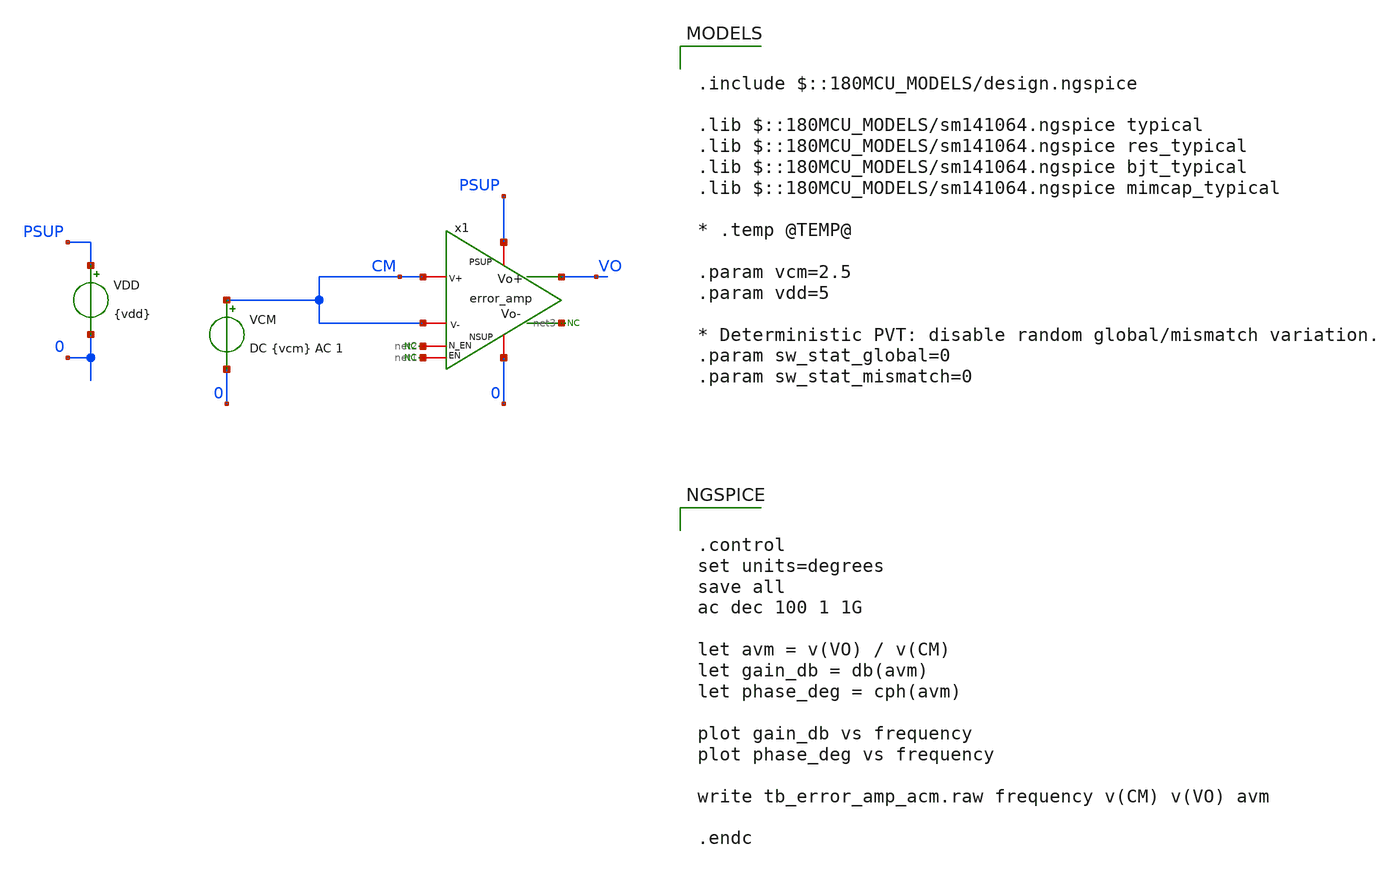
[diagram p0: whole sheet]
** sch_path: xschem/blocks/error_amp/tb_error_amp_acm.sch
**.subckt tb_error_amp_acm
VDD PSUP 0 {vdd}
VCM CM 0 DC {vcm} AC 1
* noconn #net1
* noconn #net2
x1 PSUP CM CM net2 0 net1 net3 VO error_amp
* noconn #net3
**** begin user architecture code

.include $::180MCU_MODELS/design.ngspice

.lib $::180MCU_MODELS/sm141064.ngspice typical
.lib $::180MCU_MODELS/sm141064.ngspice res_typical
.lib $::180MCU_MODELS/sm141064.ngspice bjt_typical
.lib $::180MCU_MODELS/sm141064.ngspice mimcap_typical

* .temp @TEMP@

.param vcm=2.5
.param vdd=5

* Deterministic PVT: disable random global/mismatch variation.
.param sw_stat_global=0
.param sw_stat_mismatch=0



.control
set units=degrees
save all
ac dec 100 1 1G

let avm = v(VO) / v(CM)
let gain_db = db(avm)
let phase_deg = cph(avm)

plot gain_db vs frequency
plot phase_deg vs frequency

write tb_error_amp_acm.raw frequency v(CM) v(VO) avm

.endc


**** end user architecture code
**.ends

* expanding   symbol:  blocks/error_amp/error_amp.sym # of pins=8
** sym_path: xschem/blocks/error_amp/error_amp.sym
** sch_path: xschem/blocks/error_amp/error_amp.sch
.subckt error_amp PSUP V+ V- N_EN NSUP EN Vo- Vo+
*.ipin PSUP
*.ipin NSUP
*.ipin N_EN
*.ipin EN
*.ipin V+
*.ipin V-
*.opin Vo-
*.opin Vo+
XM5 AA1 vb1 PSUP PSUP pfet_06v0 L=4u W=2u nf=4 ad='int((nf+1)/2) * W/nf * 0.18u' as='int((nf+2)/2) * W/nf * 0.18u'
+ pd='2*int((nf+1)/2) * (W/nf + 0.18u)' ps='2*int((nf+2)/2) * (W/nf + 0.18u)' nrd='0.18u / W' nrs='0.18u / W'
+ sa=0 sb=0 sd=0 m=2
XM6 AA2 vb1 PSUP PSUP pfet_06v0 L=4u W=2u nf=4 ad='int((nf+1)/2) * W/nf * 0.18u' as='int((nf+2)/2) * W/nf * 0.18u'
+ pd='2*int((nf+1)/2) * (W/nf + 0.18u)' ps='2*int((nf+2)/2) * (W/nf + 0.18u)' nrd='0.18u / W' nrs='0.18u / W'
+ sa=0 sb=0 sd=0 m=2
* noconn N_EN
* noconn EN
XM1 AA4 V- AA5 NSUP nfet_06v0 L=2u W=4u nf=5 ad='int((nf+1)/2) * W/nf * 0.18u' as='int((nf+2)/2) * W/nf * 0.18u'
+ pd='2*int((nf+1)/2) * (W/nf + 0.18u)' ps='2*int((nf+2)/2) * (W/nf + 0.18u)' nrd='0.18u / W' nrs='0.18u / W'
+ sa=0 sb=0 sd=0 m=4
XM4 mirror mirror NSUP NSUP nfet_06v0 L=4u W=2u nf=2 ad='int((nf+1)/2) * W/nf * 0.18u' as='int((nf+2)/2) * W/nf * 0.18u'
+ pd='2*int((nf+1)/2) * (W/nf + 0.18u)' ps='2*int((nf+2)/2) * (W/nf + 0.18u)' nrd='0.18u / W' nrs='0.18u / W'
+ sa=0 sb=0 sd=0 m=1
I0 vb2 mirror 1u
XM7 AA5 mirror NSUP NSUP nfet_06v0 L=4u W=2u nf=4 ad='int((nf+1)/2) * W/nf * 0.18u' as='int((nf+2)/2) * W/nf * 0.18u'
+ pd='2*int((nf+1)/2) * (W/nf + 0.18u)' ps='2*int((nf+2)/2) * (W/nf + 0.18u)' nrd='0.18u / W' nrs='0.18u / W'
+ sa=0 sb=0 sd=0 m=2
XM3 vb1 vb1 PSUP PSUP pfet_06v0 L=4u W=2u nf=1 ad='int((nf+1)/2) * W/nf * 0.18u' as='int((nf+2)/2) * W/nf * 0.18u'
+ pd='2*int((nf+1)/2) * (W/nf + 0.18u)' ps='2*int((nf+2)/2) * (W/nf + 0.18u)' nrd='0.18u / W' nrs='0.18u / W'
+ sa=0 sb=0 sd=0 m=2
XM8 Vo+ vb2 AA1 AA1 pfet_06v0 L=4u W=2u nf=4 ad='int((nf+1)/2) * W/nf * 0.18u' as='int((nf+2)/2) * W/nf * 0.18u'
+ pd='2*int((nf+1)/2) * (W/nf + 0.18u)' ps='2*int((nf+2)/2) * (W/nf + 0.18u)' nrd='0.18u / W' nrs='0.18u / W'
+ sa=0 sb=0 sd=0 m=2
XM9 Vo- vb2 AA2 AA2 pfet_06v0 L=4u W=2u nf=4 ad='int((nf+1)/2) * W/nf * 0.18u' as='int((nf+2)/2) * W/nf * 0.18u'
+ pd='2*int((nf+1)/2) * (W/nf + 0.18u)' ps='2*int((nf+2)/2) * (W/nf + 0.18u)' nrd='0.18u / W' nrs='0.18u / W'
+ sa=0 sb=0 sd=0 m=2
XM10 vb2 vb2 vb1 vb1 pfet_06v0 L=4u W=2u nf=1 ad='int((nf+1)/2) * W/nf * 0.18u' as='int((nf+2)/2) * W/nf * 0.18u'
+ pd='2*int((nf+1)/2) * (W/nf + 0.18u)' ps='2*int((nf+2)/2) * (W/nf + 0.18u)' nrd='0.18u / W' nrs='0.18u / W'
+ sa=0 sb=0 sd=0 m=2
XM2 AA3 V+ AA5 NSUP nfet_06v0 L=2u W=4u nf=5 ad='int((nf+1)/2) * W/nf * 0.18u' as='int((nf+2)/2) * W/nf * 0.18u'
+ pd='2*int((nf+1)/2) * (W/nf + 0.18u)' ps='2*int((nf+2)/2) * (W/nf + 0.18u)' nrd='0.18u / W' nrs='0.18u / W'
+ sa=0 sb=0 sd=0 m=4
XM11 Vo+ vb2 AA3 AA3 nfet_06v0 L=4u W=2u nf=4 ad='int((nf+1)/2) * W/nf * 0.18u' as='int((nf+2)/2) * W/nf * 0.18u'
+ pd='2*int((nf+1)/2) * (W/nf + 0.18u)' ps='2*int((nf+2)/2) * (W/nf + 0.18u)' nrd='0.18u / W' nrs='0.18u / W'
+ sa=0 sb=0 sd=0 m=2
XM12 Vo- vb2 AA4 AA4 nfet_06v0 L=4u W=2u nf=4 ad='int((nf+1)/2) * W/nf * 0.18u' as='int((nf+2)/2) * W/nf * 0.18u'
+ pd='2*int((nf+1)/2) * (W/nf + 0.18u)' ps='2*int((nf+2)/2) * (W/nf + 0.18u)' nrd='0.18u / W' nrs='0.18u / W'
+ sa=0 sb=0 sd=0 m=2
.ends

.end
